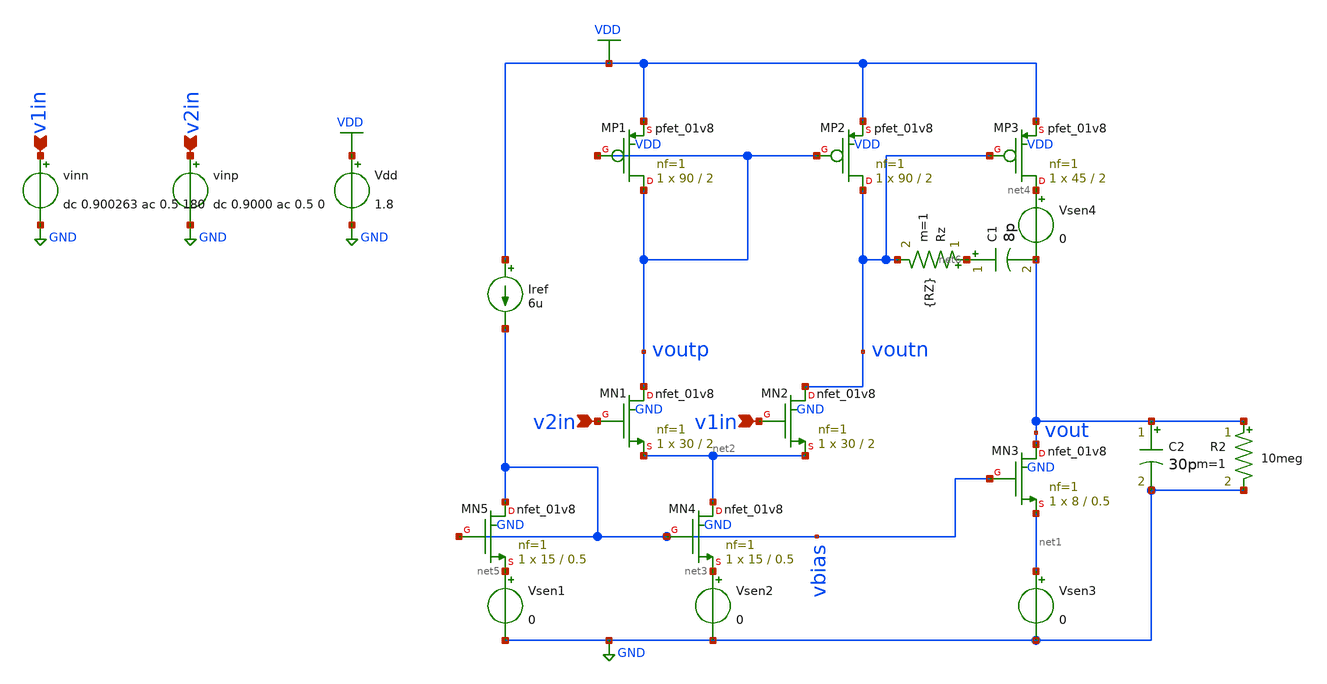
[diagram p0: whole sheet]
** sch_path: testbenches/prelayout/diffpairOL.sch
**.subckt diffpairOL v2in v1in v1in v2in
*.ipin v2in
*.ipin v1in
*.ipin v1in
*.ipin v2in
Vdd VDD GND 1.8
vinp v2in GND dc 0.9000 ac 0.5 0
vinn v1in GND dc 0.900263 ac 0.5 180
XMN1 voutp v2in net2 GND sky130_fd_pr__nfet_01v8 L=2 W=30 nf=1 ad='int((nf+1)/2) * W/nf * 0.29' as='int((nf+2)/2) * W/nf * 0.29'
+ pd='2*int((nf+1)/2) * (W/nf + 0.29)' ps='2*int((nf+2)/2) * (W/nf + 0.29)' nrd='0.29 / W' nrs='0.29 / W'
+ sa=0 sb=0 sd=0 mult=1 m=1
XMN2 voutn v1in net2 GND sky130_fd_pr__nfet_01v8 L=2 W=30 nf=1 ad='int((nf+1)/2) * W/nf * 0.29' as='int((nf+2)/2) * W/nf * 0.29'
+ pd='2*int((nf+1)/2) * (W/nf + 0.29)' ps='2*int((nf+2)/2) * (W/nf + 0.29)' nrd='0.29 / W' nrs='0.29 / W'
+ sa=0 sb=0 sd=0 mult=1 m=1
XMP1 voutp voutp VDD VDD sky130_fd_pr__pfet_01v8 L=2 W=90 nf=1 ad='int((nf+1)/2) * W/nf * 0.29' as='int((nf+2)/2) * W/nf * 0.29'
+ pd='2*int((nf+1)/2) * (W/nf + 0.29)' ps='2*int((nf+2)/2) * (W/nf + 0.29)' nrd='0.29 / W' nrs='0.29 / W'
+ sa=0 sb=0 sd=0 mult=1 m=1
XMP2 voutn voutp VDD VDD sky130_fd_pr__pfet_01v8 L=2 W=90 nf=1 ad='int((nf+1)/2) * W/nf * 0.29' as='int((nf+2)/2) * W/nf * 0.29'
+ pd='2*int((nf+1)/2) * (W/nf + 0.29)' ps='2*int((nf+2)/2) * (W/nf + 0.29)' nrd='0.29 / W' nrs='0.29 / W'
+ sa=0 sb=0 sd=0 mult=1 m=1
Iref VDD vbias 6u
Vsen2 net3 GND 0
XMP3 net4 voutn VDD VDD sky130_fd_pr__pfet_01v8 L=2 W=45 nf=1 ad='int((nf+1)/2) * W/nf * 0.29' as='int((nf+2)/2) * W/nf * 0.29'
+ pd='2*int((nf+1)/2) * (W/nf + 0.29)' ps='2*int((nf+2)/2) * (W/nf + 0.29)' nrd='0.29 / W' nrs='0.29 / W'
+ sa=0 sb=0 sd=0 mult=1 m=1
XMN3 vout vbias net1 GND sky130_fd_pr__nfet_01v8 L=0.5 W=8 nf=1 ad='int((nf+1)/2) * W/nf * 0.29' as='int((nf+2)/2) * W/nf * 0.29'
+ pd='2*int((nf+1)/2) * (W/nf + 0.29)' ps='2*int((nf+2)/2) * (W/nf + 0.29)' nrd='0.29 / W' nrs='0.29 / W'
+ sa=0 sb=0 sd=0 mult=1 m=1
Vsen3 net1 GND 0
Vsen1 net5 GND 0
C1 net6 vout 8p m=1
XMN4 net2 vbias net3 GND sky130_fd_pr__nfet_01v8 L=0.5 W=15 nf=1 ad='int((nf+1)/2) * W/nf * 0.29' as='int((nf+2)/2) * W/nf * 0.29'
+ pd='2*int((nf+1)/2) * (W/nf + 0.29)' ps='2*int((nf+2)/2) * (W/nf + 0.29)' nrd='0.29 / W' nrs='0.29 / W'
+ sa=0 sb=0 sd=0 mult=1 m=1
XMN5 vbias vbias net5 GND sky130_fd_pr__nfet_01v8 L=0.5 W=15 nf=1 ad='int((nf+1)/2) * W/nf * 0.29' as='int((nf+2)/2) * W/nf * 0.29'
+ pd='2*int((nf+1)/2) * (W/nf + 0.29)' ps='2*int((nf+2)/2) * (W/nf + 0.29)' nrd='0.29 / W' nrs='0.29 / W'
+ sa=0 sb=0 sd=0 mult=1 m=1
C2 vout GND 30p m=1
Rz net6 voutn {RZ} m=1
Vsen4 net4 vout 0
R2 vout GND 10meg m=1
**** begin user architecture code


.lib /home/ttuser/pdk/sky130A/libs.tech/ngspice/sky130.lib.spice tt

.param RZ=20.5k
.control
echo RZ DC_gain_dB UGF_Hz Phase_at_UGF_deg Phase_margin_deg >
+ /home/ttuser/projects/xschem_test/rz_Cc8p_sweep.txt


foreach rval 60k 65k 70k 75k 80k 85k 90k

    alterparam RZ=$rval
    reset
    save all

    op

    echo =================================
    echo RZ = $rval
    print v(vout)

    ac dec 100 1 10G

    let vid = v(v2in)-v(v1in)

    * Minus sign corrects the amplifier polarity
    let av = -v(vout)/vid

    let av_db = db(av)
    let av_phase = cph(av)*180/3.141592653589793

    meas ac dc_gain_db find av_db at=1
    meas ac phase_low find av_phase at=1
    meas ac ugf when av_db=0 fall=1
    meas ac phase_at_ugf find av_phase at=ugf

    let phase_margin = 180 + phase_at_ugf

    print dc_gain_db
    print phase_low
    print ugf
    print phase_at_ugf
    print phase_margin

echo $rval $&dc_gain_db $&ugf $&phase_at_ugf $&phase_margin >>
+ /home/ttuser/projects/xschem_test/rz_Cc8p_sweep.txt
end
.endc


**** end user architecture code
**.ends
.GLOBAL VDD
.GLOBAL GND
.end
